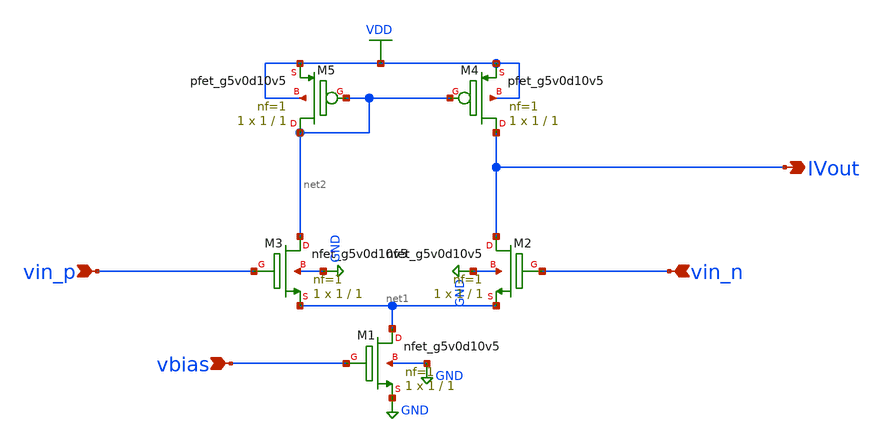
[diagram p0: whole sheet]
** sch_path: schematics/transamp_1.sch
**.subckt transamp_1 IVout vin_p vin_n vbias
*.opin IVout
*.ipin vin_p
*.ipin vin_n
*.ipin vbias
XM1 net1 vbias GND GND sky130_fd_pr__nfet_g5v0d10v5 L=1 W=1 nf=1 ad='int((nf+1)/2) * W/nf * 0.29' as='int((nf+2)/2) * W/nf * 0.29'
+ pd='2*int((nf+1)/2) * (W/nf + 0.29)' ps='2*int((nf+2)/2) * (W/nf + 0.29)' nrd='0.29 / W' nrs='0.29 / W'
+ sa=0 sb=0 sd=0 mult=1 m=1
XM3 net2 vin_p net1 GND sky130_fd_pr__nfet_g5v0d10v5 L=1 W=1 nf=1 ad='int((nf+1)/2) * W/nf * 0.29' as='int((nf+2)/2) * W/nf * 0.29'
+ pd='2*int((nf+1)/2) * (W/nf + 0.29)' ps='2*int((nf+2)/2) * (W/nf + 0.29)' nrd='0.29 / W' nrs='0.29 / W'
+ sa=0 sb=0 sd=0 mult=1 m=1
XM4 IVout net2 VDD VDD sky130_fd_pr__pfet_g5v0d10v5 L=1 W=1 nf=1 ad='int((nf+1)/2) * W/nf * 0.29' as='int((nf+2)/2) * W/nf * 0.29'
+ pd='2*int((nf+1)/2) * (W/nf + 0.29)' ps='2*int((nf+2)/2) * (W/nf + 0.29)' nrd='0.29 / W' nrs='0.29 / W'
+ sa=0 sb=0 sd=0 mult=1 m=1
XM2 IVout vin_n net1 GND sky130_fd_pr__nfet_g5v0d10v5 L=1 W=1 nf=1 ad='int((nf+1)/2) * W/nf * 0.29' as='int((nf+2)/2) * W/nf * 0.29'
+ pd='2*int((nf+1)/2) * (W/nf + 0.29)' ps='2*int((nf+2)/2) * (W/nf + 0.29)' nrd='0.29 / W' nrs='0.29 / W'
+ sa=0 sb=0 sd=0 mult=1 m=1
XM5 net2 net2 VDD VDD sky130_fd_pr__pfet_g5v0d10v5 L=1 W=1 nf=1 ad='int((nf+1)/2) * W/nf * 0.29' as='int((nf+2)/2) * W/nf * 0.29'
+ pd='2*int((nf+1)/2) * (W/nf + 0.29)' ps='2*int((nf+2)/2) * (W/nf + 0.29)' nrd='0.29 / W' nrs='0.29 / W'
+ sa=0 sb=0 sd=0 mult=1 m=1
**.ends
.GLOBAL GND
.GLOBAL VDD
.end
